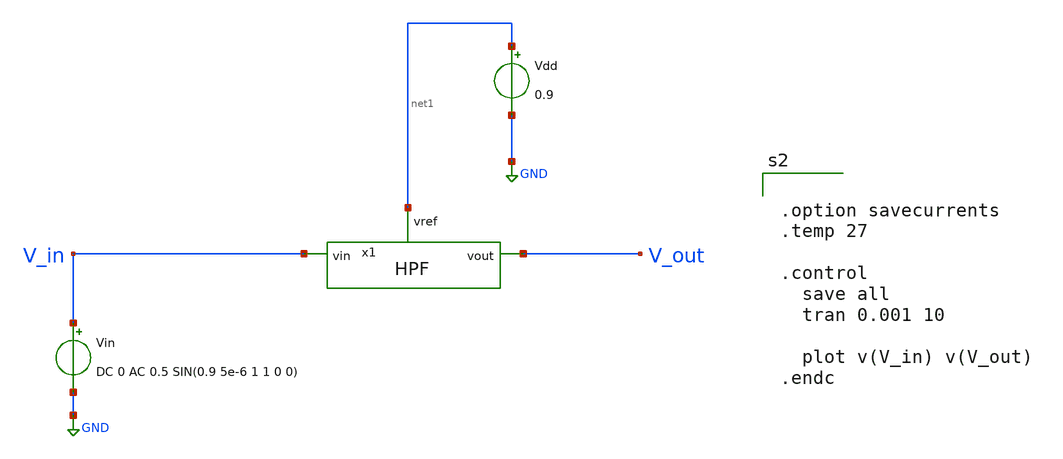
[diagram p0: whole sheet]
** sch_path: Schematic/HPF_Trans_tb.sch
**.subckt HPF_Trans_tb
Vin V_in GND DC 0 AC 0.5 SIN(0.9 5e-6 1 1 0 0)
Vdd net1 GND 0.9
x1 net1 V_out V_in HPF
**** begin user architecture code

** opencircuitdesign pdks install
.lib $::SKYWATER_MODELS/sky130.lib.spice tt




.option savecurrents
.temp 27

.control
  save all
  tran 0.001 10

  plot v(V_in) v(V_out)
.endc



**** end user architecture code
**.ends

* expanding   symbol:  /foss/designs/Analog_to_Spike/Schematic/HPF.sym # of pins=3
** sym_path: Schematic/HPF.sym
** sch_path: Schematic/HPF.sch
.subckt HPF vref vout vin
*.ipin vin
*.opin vout
*.ipin vref
XC1 vout vin sky130_fd_pr__cap_mim_m3_1 W=12 L=12 MF=2 m=2
XM1 vout net1 net1 vref sky130_fd_pr__pfet_01v8 L=1 W=1 nf=1 ad='int((nf+1)/2) * W/nf * 0.29' as='int((nf+2)/2) * W/nf * 0.29'
+ pd='2*int((nf+1)/2) * (W/nf + 0.29)' ps='2*int((nf+2)/2) * (W/nf + 0.29)' nrd='0.29 / W' nrs='0.29 / W'
+ sa=0 sb=0 sd=0 mult=1 m=1
XM2 net1 net1 vref vref sky130_fd_pr__pfet_01v8 L=1 W=1 nf=1 ad='int((nf+1)/2) * W/nf * 0.29' as='int((nf+2)/2) * W/nf * 0.29'
+ pd='2*int((nf+1)/2) * (W/nf + 0.29)' ps='2*int((nf+2)/2) * (W/nf + 0.29)' nrd='0.29 / W' nrs='0.29 / W'
+ sa=0 sb=0 sd=0 mult=1 m=1
.ends

.GLOBAL GND
.end
